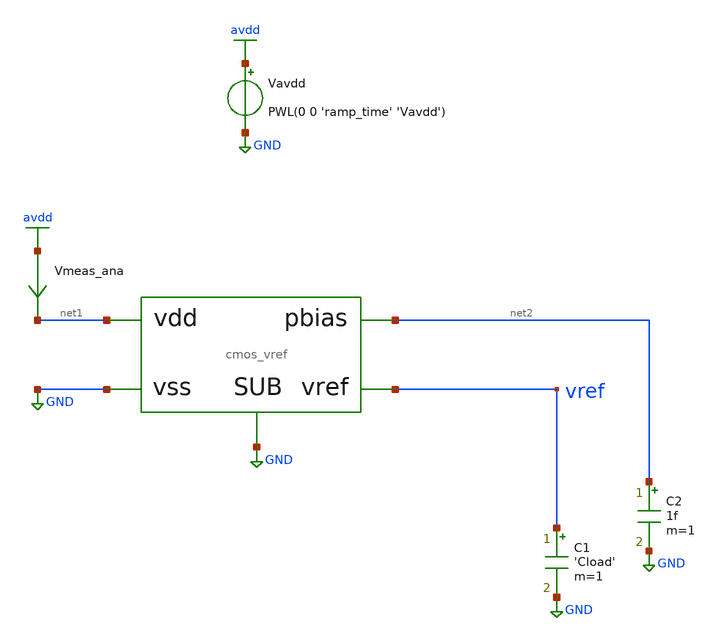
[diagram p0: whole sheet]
** sch_path: tb/cmos_vref/tb_vref_startup.sch
**.subckt tb_vref_startup
Vavdd avdd GND PWL(0 0 'ramp_time' 'Vavdd')
C1 vref GND 'Cload' m=1
Vmeas_ana avdd net1 0
.save i(vmeas_ana)
X1 vref net1 GND net2 GND cmos_vref
C2 net2 GND 1f m=1
**** begin user architecture code


.lib 'models_dir'/cornerMOShv.lib 'mos_corner'
.lib 'models_dir'/cornerMOSlv.lib 'mos_corner'
.lib 'models_dir'/cornerCAP.lib cap_typ
.option TEMP='temperature'
.option warn=1
.control
save all
tran 10n 1500u 0 100n
let vds_m6 = v(x1.net2) - v(x1.vptat)
let vds_m7 = v(x1.net3)
set wr_singlescale
wrdata 'simpath'/'filename'_'N'.data V(vref)
wrdata 'simpath'/'filename'_'N'_diag.data v(vref) v(x1.vptat) v(x1.vbias_st) v(net2) v(x1.net4) vds_m6
+ vds_m7 i(v.x1.vm_b1) i(vmeas_ana)
set filetype=ascii
write 'simpath'/'filename'_'N'.raw
quit
.endc


**** end user architecture code
**.ends

* expanding   symbol:  sch/cmos_vref.sym # of pins=5
** sym_path: release/xschem/sch/cmos_vref.sym
** sch_path: release/xschem/sch/cmos_vref.sch
.subckt cmos_vref vref vdd vss pbias SUB
*.iopin vss
*.iopin SUB
*.iopin vdd
*.opin pbias
*.opin vref
Vm_b1 vdd net1 0
.save i(vm_b1)
XM1 vptat vref vss SUB sg13_hv_nmos w=2.5u l=20u ng=1 m=1 mm_ok=1
XM2 vref vref vptat SUB sg13_hv_nmos w=2u l=10u ng=1 m=1 mm_ok=1
XM3 vref pbias net1 vdd sg13_hv_pmos w=50u l=10u ng=1 m=1 mm_ok=1
Vm_st1 pbias net5 0
.save i(vm_st1)
Vm_st2 vdd net6 0
.save i(vm_st2)
Vm_b3 vdd net7 0
.save i(vm_b3)
Vm_b4 vdd net8 0
.save i(vm_b4)
XM7 net3 vbias_st vss SUB sg13_hv_nmos w=5u l=2u ng=1 m=1 mm_ok=1
XM11 vbias_st pbias net8 vdd sg13_hv_pmos w=5u l=10u ng=1 m=1 mm_ok=1
XM6 net2 vbias_st vptat SUB sg13_hv_nmos w=100u l=2u ng=1 m=1 mm_ok=1
XM9 vbias_st vref net3 SUB sg13_hv_nmos w=10u l=10u ng=1 m=1 mm_ok=1
XM8 pbias vref net2 SUB sg13_hv_nmos w=10u l=10u ng=1 m=1 mm_ok=1
XM10 pbias pbias net7 vdd sg13_hv_pmos w=5u l=10u ng=1 m=1 mm_ok=1
XM13 net4 vbias_st vss SUB sg13_hv_nmos w=10u l=5u ng=1 m=1 mm_ok=1
XM12 net5 net4 vss SUB sg13_hv_nmos w=5u l=10u ng=1 m=1 mm_ok=1
XC1 net6 net4 cap_cmim w=7u l=7u m=10 mm_ok=1
.ends

.GLOBAL avdd
.GLOBAL GND
.end
